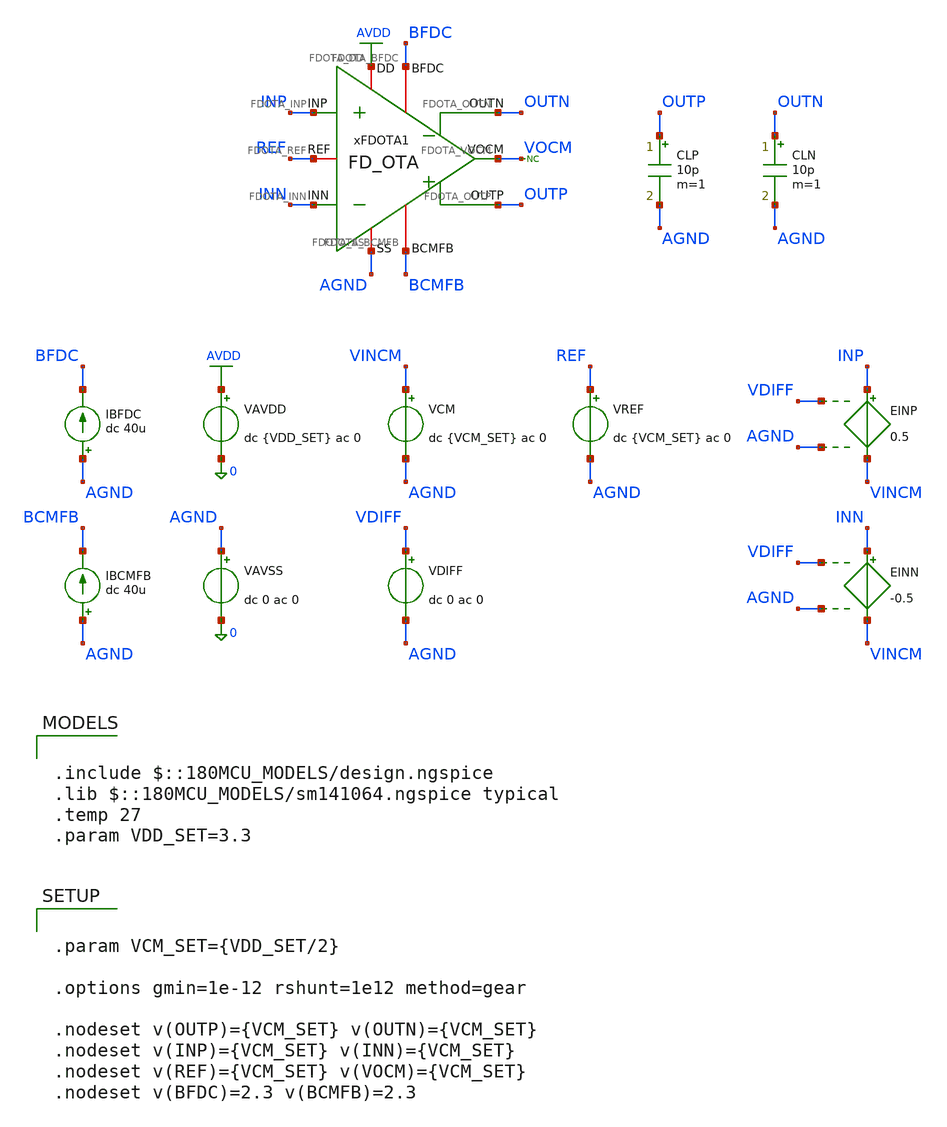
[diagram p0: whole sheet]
** sch_path: Design_Files/IC Design/Testbench/FD_OTA/FDOTA old/FD_OTA_TB_ICMR_NOM.sch
**.subckt FD_OTA_TB_ICMR_NOM
IBFDC AGND BFDC dc 40u
VAVDD AVDD 0 dc {VDD_SET} ac 0
.save i(vavdd)
VCM VINCM AGND dc {VCM_SET} ac 0
VDIFF VDIFF AGND dc 0 ac 0
VAVSS AGND 0 dc 0 ac 0
.save i(vavss)
VREF REF AGND dc {VCM_SET} ac 0
EINP INP VINCM VDIFF AGND 0.5
EINN INN VINCM VDIFF AGND -0.5
IBCMFB AGND BCMFB dc 40u
CLP OUTP AGND 10p m=1
CLN OUTN AGND 10p m=1
* noconn VOCM
xFDOTA1 AVDD AGND INP INN OUTN BFDC OUTP BCMFB REF VOCM FD_OTA
**** begin user architecture code

.include $::180MCU_MODELS/design.ngspice
.lib $::180MCU_MODELS/sm141064.ngspice typical
.temp 27
.param VDD_SET=3.3




.control
destroy all
save all
set wr_vecnames
set wr_singlescale
option numdgt=15

shell mkdir -p
+ /foss/designs/ECG_Acquisition_IC/Measurement_Results/IC_Simulation/FD_OTA/FDOTA/NOM.Result_txt

shell rm -f
+ /foss/designs/ECG_Acquisition_IC/Measurement_Results/IC_Simulation/FD_OTA/FDOTA/NOM.Result_txt/NOM.icmr_op.txt
shell rm -f
+ /foss/designs/ECG_Acquisition_IC/Measurement_Results/IC_Simulation/FD_OTA/FDOTA/NOM.Result_txt/NOM.cl_icmr.txt

* OP
op

let avdd_run = v(AVDD)-v(AGND)
let vcm_run = avdd_run/2

alter @VREF[DC] = $&vcm_run
alter @VCM[DC] = $&vcm_run
alter @VDIFF[DC] = 0

op

let op_voutcm = 0.5*(v(OUTP)+v(OUTN))
let op_voutdiff = v(OUTP)-v(OUTN)
let op_idd = -vavdd#branch

wrdata
+ /foss/designs/ECG_Acquisition_IC/Measurement_Results/IC_Simulation/FD_OTA/FDOTA/NOM.Result_txt/NOM.icmr_op.txt v(REF) v(VOCM) v(BCMFB) v(INP) v(INN) v(OUTP) v(OUTN) op_voutcm op_voutdiff op_idd

* ICMR
let vcm_low_sweep = 0
let vcm_high_sweep = avdd_run

dc VCM $&vcm_low_sweep $&vcm_high_sweep 0.05 VDIFF -50m 50m 0.5m

let icmr_vin_cm = 0.5*(v(INP)+v(INN))
let icmr_vin_diff = v(INP)-v(INN)
let icmr_voutcm = 0.5*(v(OUTP)+v(OUTN))
let icmr_voutdiff = v(OUTP)-v(OUTN)
let icmr_idd = -vavdd#branch

setscale icmr_vin_cm

wrdata
+ /foss/designs/ECG_Acquisition_IC/Measurement_Results/IC_Simulation/FD_OTA/FDOTA/NOM.Result_txt/NOM.cl_icmr.txt v(VINCM) v(REF) v(BCMFB) icmr_vin_diff v(INP) v(INN) v(OUTP) v(OUTN) icmr_voutcm icmr_voutdiff
+ v(VOCM) icmr_idd

quit
.endc




.param VCM_SET={VDD_SET/2}

.options gmin=1e-12 rshunt=1e12 method=gear

.nodeset v(OUTP)={VCM_SET} v(OUTN)={VCM_SET}
.nodeset v(INP)={VCM_SET} v(INN)={VCM_SET}
.nodeset v(REF)={VCM_SET} v(VOCM)={VCM_SET}
.nodeset v(BFDC)=2.3 v(BCMFB)=2.3


**** end user architecture code
**.ends
.GLOBAL AVDD
.end
